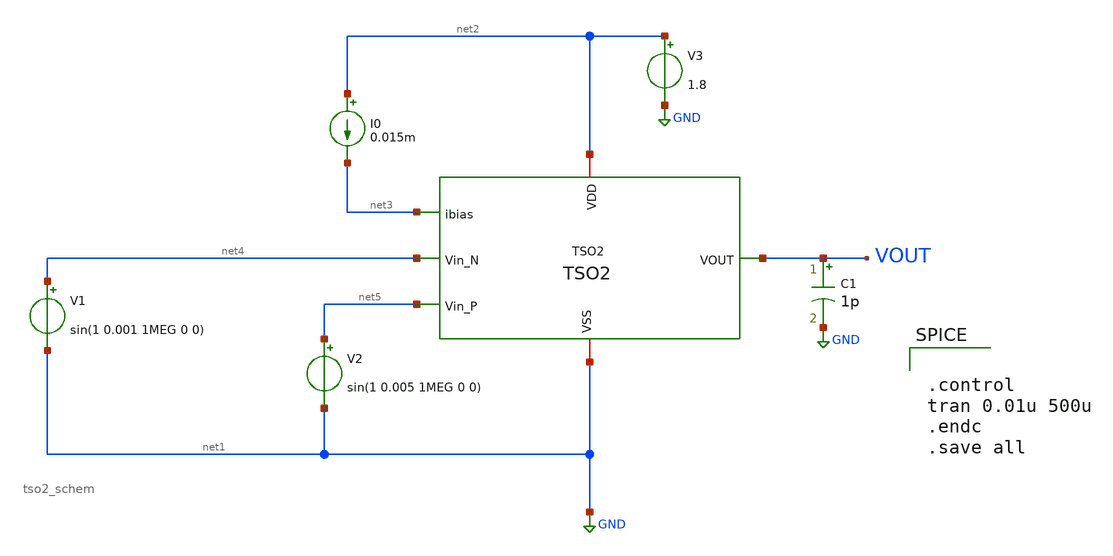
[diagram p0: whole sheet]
** sch_path: xschem/untitled-5.sch
**.subckt untitled-5
x1 net6 net4 net5 net3 net1 net2 tso2_schem
I0 net7 net3 0.015m
V1 net4 net1 sin(1 0.001 1MEG 0 0)
V2 net5 net1 sin(1 0.005 1MEG 0 0)
V3 net2 GND 1.8
C1 VOUT GND 1p m=1
**** begin user architecture code

** opencircuitdesign pdks install
.lib $::SKYWATER_MODELS/sky130.lib.spice tt




.control
tran 0.01u 500u
.endc
.save all


**** end user architecture code
**.ends

* expanding   symbol:  tso2_schem.sym # of pins=6
** sym_path: xschem/tso2_schem.sym
** sch_path: xschem/tso2_schem.sch
.subckt tso2_schem VOUT Vin_N Vin_P ibias VSS VDD
*.opin VOUT
*.iopin VDD
*.iopin VSS
*.ipin ibias
*.ipin Vin_P
*.ipin Vin_N
XM1 net4 Vin_N vs1 GND sky130_fd_pr__nfet_01v8 L=0.5 W=1.5 nf=1 ad='int((nf+1)/2) * W/nf * 0.29' as='int((nf+2)/2) * W/nf * 0.29'
+ pd='2*int((nf+1)/2) * (W/nf + 0.29)' ps='2*int((nf+2)/2) * (W/nf + 0.29)' nrd='0.29 / W' nrs='0.29 / W'
+ sa=0 sb=0 sd=0 mult=1 m=1
XM2 net3 Vin_P vs1 GND sky130_fd_pr__nfet_01v8 L=0.5 W=1.5 nf=1 ad='int((nf+1)/2) * W/nf * 0.29' as='int((nf+2)/2) * W/nf * 0.29'
+ pd='2*int((nf+1)/2) * (W/nf + 0.29)' ps='2*int((nf+2)/2) * (W/nf + 0.29)' nrd='0.29 / W' nrs='0.29 / W'
+ sa=0 sb=0 sd=0 mult=1 m=1
XM3 vd1 vd1 VDD VDD sky130_fd_pr__pfet_01v8 L=0.5 W=1.5 nf=1 ad='int((nf+1)/2) * W/nf * 0.29' as='int((nf+2)/2) * W/nf * 0.29'
+ pd='2*int((nf+1)/2) * (W/nf + 0.29)' ps='2*int((nf+2)/2) * (W/nf + 0.29)' nrd='0.29 / W' nrs='0.29 / W'
+ sa=0 sb=0 sd=0 mult=1 m=1
XM4 vd2 vd1 VDD VDD sky130_fd_pr__pfet_01v8 L=0.5 W=1.5 nf=1 ad='int((nf+1)/2) * W/nf * 0.29' as='int((nf+2)/2) * W/nf * 0.29'
+ pd='2*int((nf+1)/2) * (W/nf + 0.29)' ps='2*int((nf+2)/2) * (W/nf + 0.29)' nrd='0.29 / W' nrs='0.29 / W'
+ sa=0 sb=0 sd=0 mult=1 m=1
XM5 net2 ibias VSS VSS sky130_fd_pr__nfet_01v8 L=0.5 W=4 nf=1 ad='int((nf+1)/2) * W/nf * 0.29' as='int((nf+2)/2) * W/nf * 0.29'
+ pd='2*int((nf+1)/2) * (W/nf + 0.29)' ps='2*int((nf+2)/2) * (W/nf + 0.29)' nrd='0.29 / W' nrs='0.29 / W'
+ sa=0 sb=0 sd=0 mult=1 m=1
XM6 net1 vg6 VDD VDD sky130_fd_pr__pfet_01v8 L=0.5 W=30 nf=1 ad='int((nf+1)/2) * W/nf * 0.29' as='int((nf+2)/2) * W/nf * 0.29'
+ pd='2*int((nf+1)/2) * (W/nf + 0.29)' ps='2*int((nf+2)/2) * (W/nf + 0.29)' nrd='0.29 / W' nrs='0.29 / W'
+ sa=0 sb=0 sd=0 mult=1 m=1
XM7 VOUT ibias VSS VSS sky130_fd_pr__nfet_01v8 L=1.75 W=36 nf=1 ad='int((nf+1)/2) * W/nf * 0.29' as='int((nf+2)/2) * W/nf * 0.29'
+ pd='2*int((nf+1)/2) * (W/nf + 0.29)' ps='2*int((nf+2)/2) * (W/nf + 0.29)' nrd='0.29 / W' nrs='0.29 / W'
+ sa=0 sb=0 sd=0 mult=1 m=1
XM8 ibias ibias VSS VSS sky130_fd_pr__nfet_01v8 L=0.5 W=4 nf=1 ad='int((nf+1)/2) * W/nf * 0.29' as='int((nf+2)/2) * W/nf * 0.29'
+ pd='2*int((nf+1)/2) * (W/nf + 0.29)' ps='2*int((nf+2)/2) * (W/nf + 0.29)' nrd='0.29 / W' nrs='0.29 / W'
+ sa=0 sb=0 sd=0 mult=1 m=1
XC1 vg6 net1 sky130_fd_pr__cap_mim_m3_1 W=19.4 L=19.4 MF=4 m=4
XC2 VOUT VSS sky130_fd_pr__cap_mim_m3_1 W=25 L=25 MF=8 m=8
v5 vd1 net4 0
.save i(v5)
v1 vs1 net2 0
.save i(v1)
v2 vd2 net3 0
.save i(v2)
v3 vd2 vg6 0
.save i(v3)
v4 net1 VOUT 0
.save i(v4)
.ends

.GLOBAL GND
.end
